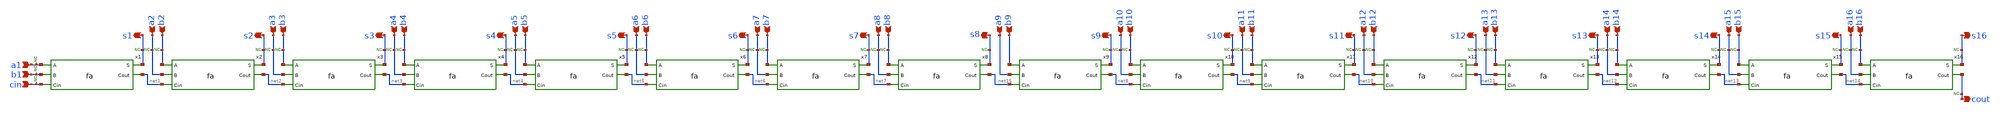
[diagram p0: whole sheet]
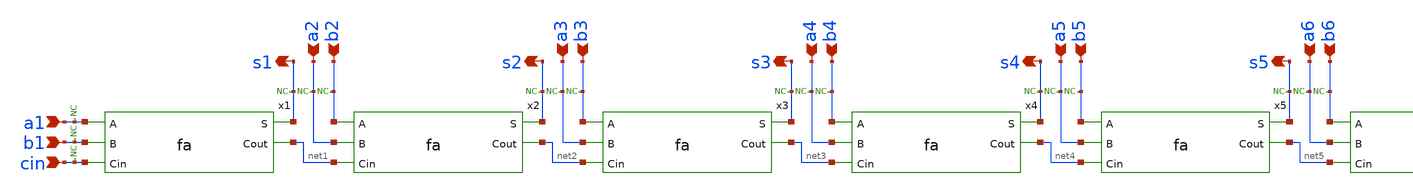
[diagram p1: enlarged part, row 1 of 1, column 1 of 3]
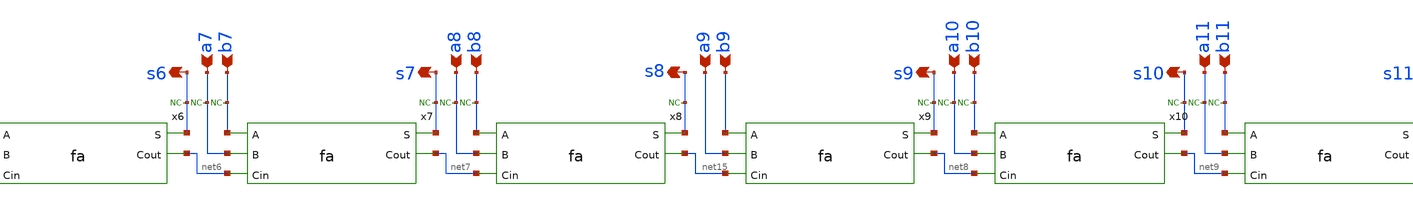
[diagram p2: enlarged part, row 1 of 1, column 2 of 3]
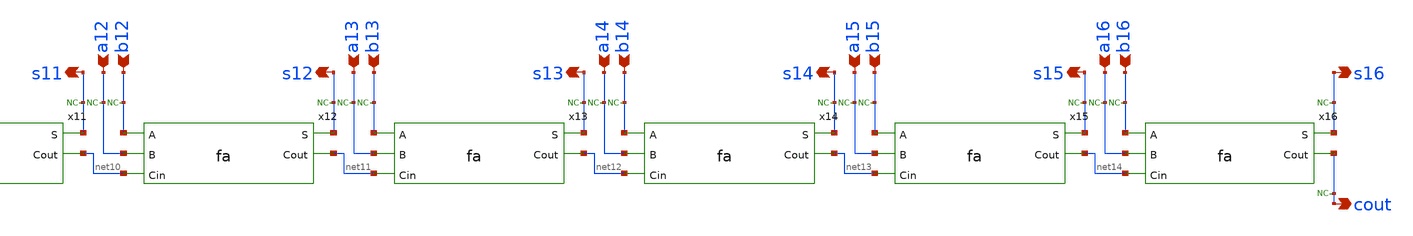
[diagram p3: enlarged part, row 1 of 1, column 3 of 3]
** sch_path: tut7/rca16.sch
**.subckt rca16 a1 b1 cin a2 b2 a3 b3 a4 b4 a5 b5 a6 b6 a7 b7 a8 b8 s8 s7 s6 s5 s4 s3 s2 s1 a10 b10
*+ a11 b11 a12 b12 a13 b13 a14 b14 a15 b15 a16 b16 cout s16 s15 s14 s13 s12 s11 s10 s9 a9 b9
*.ipin a1
*.ipin b1
*.ipin cin
*.ipin a2
*.ipin b2
*.ipin a3
*.ipin b3
*.ipin a4
*.ipin b4
*.ipin a5
*.ipin b5
*.ipin a6
*.ipin b6
*.ipin a7
*.ipin b7
*.ipin a8
*.ipin b8
*.opin s8
*.opin s7
*.opin s6
*.opin s5
*.opin s4
*.opin s3
*.opin s2
*.opin s1
*.ipin a10
*.ipin b10
*.ipin a11
*.ipin b11
*.ipin a12
*.ipin b12
*.ipin a13
*.ipin b13
*.ipin a14
*.ipin b14
*.ipin a15
*.ipin b15
*.ipin a16
*.ipin b16
*.opin cout
*.opin s16
*.opin s15
*.opin s14
*.opin s13
*.opin s12
*.opin s11
*.opin s10
*.opin s9
*.ipin a9
*.ipin b9
x1 a1 s1 b1 net1 cin fa
x2 b2 s2 a2 net2 net1 fa
x3 b3 s3 a3 net3 net2 fa
x4 b4 s4 a4 net4 net3 fa
x5 b5 s5 a5 net5 net4 fa
x6 b6 s6 a6 net6 net5 fa
x7 b7 s7 a7 net7 net6 fa
x8 b8 s8 a8 net15 net7 fa
* noconn a1
* noconn b1
* noconn cin
* noconn s1
* noconn s2
* noconn s3
* noconn s4
* noconn s5
* noconn s6
* noconn s7
* noconn s8
* noconn a2
* noconn b2
* noconn b3
* noconn a3
* noconn a4
* noconn b4
* noconn a5
* noconn b5
* noconn a6
* noconn b6
* noconn b7
* noconn a7
* noconn b8
* noconn a8
x9 b9 s9 a9 net8 net15 fa
x10 b10 s10 a10 net9 net8 fa
x11 b11 s11 a11 net10 net9 fa
x12 b12 s12 a12 net11 net10 fa
x13 b13 s13 a13 net12 net11 fa
x14 b14 s14 a14 net13 net12 fa
x15 b15 s15 a15 net14 net13 fa
x16 b16 s16 a16 cout net14 fa
* noconn s9
* noconn s10
* noconn s11
* noconn s12
* noconn s13
* noconn s14
* noconn s15
* noconn s16
* noconn cout
* noconn a10
* noconn b10
* noconn b11
* noconn a11
* noconn a12
* noconn b12
* noconn a13
* noconn b13
* noconn a14
* noconn b14
* noconn b15
* noconn a15
* noconn b16
* noconn a16
**.ends
.end
